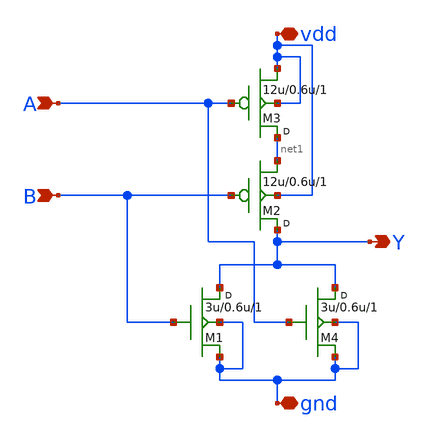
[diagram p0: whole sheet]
** sch_path: lab7/sch/nor.sch
**.subckt nor A B Y vdd gnd
*.ipin A
*.ipin B
*.opin Y
*.iopin vdd
*.iopin gnd
M3 net1 A vdd vdd pfet w=12u l=0.6u m=1
M4 Y A gnd gnd nfet w=3u l=0.6u m=1
M1 Y B gnd gnd nfet w=3u l=0.6u m=1
M2 Y B net1 vdd pfet w=12u l=0.6u m=1
**.ends
.end
